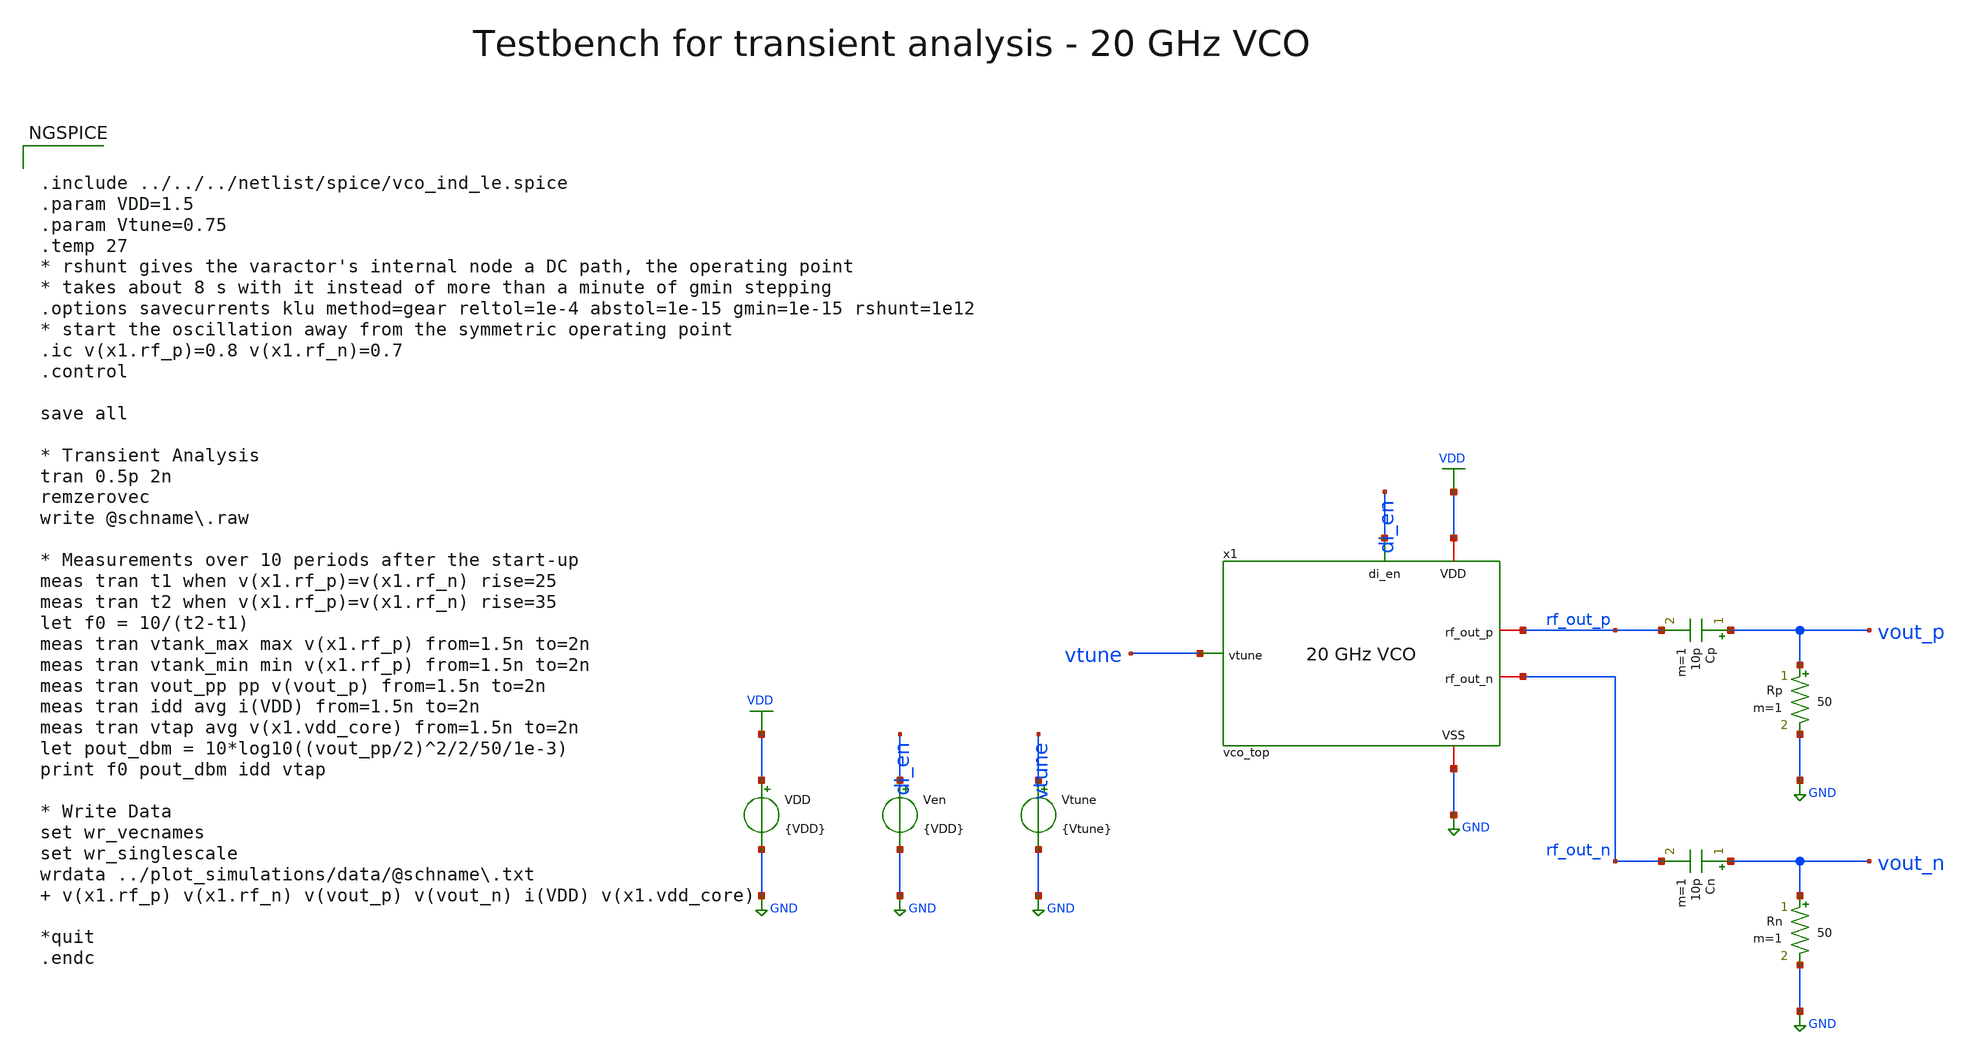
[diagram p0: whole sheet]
** sch_path: macros/vco/testbenches/xschem/vco_top_tb_tran.sch
**.subckt vco_top_tb_tran
x1 di_en VDD GND vtune rf_out_p rf_out_n vco_top
Cp vout_p rf_out_p 10p m=1
Rp vout_p GND 50 m=1
Cn vout_n rf_out_n 10p m=1
Rn vout_n GND 50 m=1
VDD VDD GND {VDD}
Ven di_en GND {VDD}
Vtune vtune GND {Vtune}
**** begin user architecture code


.include ../../../netlist/spice/vco_ind_le.spice
.param VDD=1.5
.param Vtune=0.75
.temp 27
* rshunt gives the varactor's internal node a DC path, the operating point
* takes about 8 s with it instead of more than a minute of gmin stepping
.options savecurrents klu method=gear reltol=1e-4 abstol=1e-15 gmin=1e-15 rshunt=1e12
* start the oscillation away from the symmetric operating point
.ic v(x1.rf_p)=0.8 v(x1.rf_n)=0.7
.control

save all

* Transient Analysis
tran 0.5p 2n
remzerovec
write @schname\.raw

* Measurements over 10 periods after the start-up
meas tran t1 when v(x1.rf_p)=v(x1.rf_n) rise=25
meas tran t2 when v(x1.rf_p)=v(x1.rf_n) rise=35
let f0 = 10/(t2-t1)
meas tran vtank_max max v(x1.rf_p) from=1.5n to=2n
meas tran vtank_min min v(x1.rf_p) from=1.5n to=2n
meas tran vout_pp pp v(vout_p) from=1.5n to=2n
meas tran idd avg i(VDD) from=1.5n to=2n
meas tran vtap avg v(x1.vdd_core) from=1.5n to=2n
let pout_dbm = 10*log10((vout_pp/2)^2/2/50/1e-3)
print f0 pout_dbm idd vtap

* Write Data
set wr_vecnames
set wr_singlescale
wrdata ../plot_simulations/data/@schname\.txt  v(x1.rf_p) v(x1.rf_n) v(vout_p) v(vout_n) i(VDD) v(x1.vdd_core)

*quit
.endc



.lib cornerMOSlv.lib mos_tt
.lib cornerMOShv.lib mos_tt
.lib cornerRES.lib res_typ
.lib cornerCAP.lib cap_typ

**** end user architecture code
**.ends

* expanding   symbol:  vco_top.sym # of pins=6
** sym_path: macros/vco/schematic/xschem/vco_top.sym
** sch_path: macros/vco/schematic/xschem/vco_top.sch
.subckt vco_top di_en VDD VSS vtune rf_out_p rf_out_n
*.iopin VDD
*.iopin VSS
*.ipin di_en
*.ipin vtune
*.iopin rf_out_p
*.iopin rf_out_n
xbias di_en VDD VSS vbg_buf vbn_buf en_b vco_bias
xcore vdd_core VSS vtune rf_p rf_n vco_core
xbuf vbn_buf vbg_buf VDD VSS rf_p rf_n rf_out_p rf_out_n vco_buf
xfeed en_b VDD VSS vdd_core vco_feed
.ends


* expanding   symbol:  vco_bias.sym # of pins=6
** sym_path: macros/vco/schematic/xschem/vco_bias.sym
** sch_path: macros/vco/schematic/xschem/vco_bias.sch
.subckt vco_bias di_en VDD VSS vbg_buf vbn_buf en_b
*.iopin VDD
*.iopin VSS
*.ipin di_en
*.opin en_b
*.iopin vbn_buf
*.iopin vbg_buf
XMPi1 en_b di_en VDD VDD sg13_lv_pmos w=1u l=0.13u ng=1 m=1 mm_ok=1
XMNi1 en_b di_en VSS VSS sg13_lv_nmos w=0.5u l=0.13u ng=1 m=1 mm_ok=1
XMPi2 en en_b VDD VDD sg13_lv_pmos w=1u l=0.13u ng=1 m=1 mm_ok=1
XMNi2 en en_b VSS VSS sg13_lv_nmos w=0.5u l=0.13u ng=1 m=1 mm_ok=1
XMN0 ibias_100u ibias_100u VSS VSS sg13_lv_nmos w=2.5u l=0.5u ng=1 m=1 mm_ok=1
XMNd0 ibias_100u en_b VSS VSS sg13_lv_nmos w=1u l=0.13u ng=1 m=1 mm_ok=1
XRn ibias_100u vbn_buf VSS rhigh w=0.5e-6 l=32e-6 m=1 b=0 mm_ok=1
XMNd1 vbn_buf en_b VSS VSS sg13_lv_nmos w=1u l=0.13u ng=1 m=1 mm_ok=1
XMN1 vbp_ref ibias_100u VSS VSS sg13_lv_nmos w=2.5u l=0.5u ng=1 m=1 mm_ok=1
XMP1 vbp_ref vbp_ref VDD VDD sg13_lv_pmos w=5u l=0.5u ng=1 m=1 mm_ok=1
XMPd vbp_ref en VDD VDD sg13_lv_pmos w=1u l=0.13u ng=1 m=1 mm_ok=1
XMP2 vbg_int vbp_ref VDD VDD sg13_lv_pmos w=5u l=0.5u ng=1 m=1 mm_ok=1
XRg vbg_int nbg VSS rppd w=0.5e-6 l=8.5e-6 m=1 b=0 mm_ok=1
XMN3 nbg nbg VSS VSS sg13_lv_nmos w=2.5u l=0.5u ng=1 m=1 mm_ok=1
XMCn1 VSS vbn_buf VSS VSS sg13_lv_nmos w=40u l=10u ng=5 m=1 mm_ok=1
XMCn2 VSS vbn_buf VSS VSS sg13_lv_nmos w=40u l=10u ng=5 m=1 mm_ok=1
XRf vbg_int vbg_buf VSS rhigh w=0.5e-6 l=32e-6 m=1 b=0 mm_ok=1
XMCg1 VSS vbg_buf VSS VSS sg13_lv_nmos w=40u l=10u ng=5 m=1 mm_ok=1
XMCg2 VSS vbg_buf VSS VSS sg13_lv_nmos w=40u l=10u ng=5 m=1 mm_ok=1
XMDn1 VSS VSS VSS VSS sg13_lv_nmos w=2.5u l=0.5u ng=1 m=1 mm_ok=1
XMDn2 VSS VSS VSS VSS sg13_lv_nmos w=2.5u l=0.5u ng=1 m=1 mm_ok=1
XMDp1 VDD VDD VDD VDD sg13_lv_pmos w=5u l=0.5u ng=1 m=1 mm_ok=1
XMDp2 VDD VDD VDD VDD sg13_lv_pmos w=5u l=0.5u ng=1 m=1 mm_ok=1
XMPb nrb en_b VDD VDD sg13_lv_pmos w=2u l=0.13u ng=1 m=1 mm_ok=1
XMDp4 VDD VDD VDD VDD sg13_lv_pmos w=1u l=0.13u ng=1 m=1 mm_ok=1
XRb nrb ibias_100u VSS rppd w=0.5e-6 l=13.1e-6 m=1 b=0 mm_ok=1
XCg1 vbg_buf VSS cap_cmim w=17.5e-6 l=19.1e-6 m=1 mm_ok=1
XCg2 vbg_buf VSS cap_cmim w=13.6e-6 l=7.28e-6 m=1 mm_ok=1
.ends


* expanding   symbol:  vco_core.sym # of pins=5
** sym_path: macros/vco/schematic/xschem/vco_core.sym
** sch_path: macros/vco/schematic/xschem/vco_core.sch
.subckt vco_core vdd_core VSS vtune rf_p rf_n
*.iopin vdd_core
*.iopin VSS
*.ipin vtune
*.iopin rf_p
*.iopin rf_n
xind rf_p rf_n vdd_core VSS vco_ind
XCct1 vdd_core VSS cap_cmim w=56e-6 l=39e-6 m=1 mm_ok=1
xvar rf_p rf_n vtune VSS vco_var
XM1 rf_p rf_n VSS VSS sg13_lv_nmos w=20u l=0.13u ng=10 m=1 mm_ok=1
XM2 rf_n rf_p VSS VSS sg13_lv_nmos w=20u l=0.13u ng=10 m=1 mm_ok=1
XCct2 vdd_core VSS cap_cmim w=42e-6 l=25.5e-6 m=1 mm_ok=1
.ends


* expanding   symbol:  vco_buf.sym # of pins=8
** sym_path: macros/vco/schematic/xschem/vco_buf.sym
** sch_path: macros/vco/schematic/xschem/vco_buf.sch
.subckt vco_buf vbn_buf vbg_buf VDD VSS rf_p rf_n rf_out_p rf_out_n
*.iopin VDD
*.iopin VSS
*.iopin rf_out_n
*.iopin rf_out_p
*.ipin vbn_buf
*.iopin rf_p
*.iopin rf_n
*.ipin vbg_buf
XMB1 rf_out_n gp tail VSS sg13_lv_nmos w=24u l=0.13u ng=12 m=1 mm_ok=1
XMB2 rf_out_p gn tail VSS sg13_lv_nmos w=24u l=0.13u ng=12 m=1 mm_ok=1
XRL1 VDD rf_out_n VSS rppd w=10e-6 l=1.65e-6 m=1 b=0 mm_ok=1
XRL2 VDD rf_out_p VSS rppd w=10e-6 l=1.65e-6 m=1 b=0 mm_ok=1
XMBt tail vbn_buf VSS VSS sg13_lv_nmos w=150u l=0.5u ng=30 m=1 mm_ok=1
XCc1 gp rf_p cap_cmim w=10e-6 l=10e-6 m=1 mm_ok=1
XCc2 gn rf_n cap_cmim w=10e-6 l=10e-6 m=1 mm_ok=1
XRb1 vbg_buf gp VSS rhigh w=0.5e-6 l=8e-6 m=1 b=0 mm_ok=1
XRb2 vbg_buf gn VSS rhigh w=0.5e-6 l=8e-6 m=1 b=0 mm_ok=1
.ends


* expanding   symbol:  vco_feed.sym # of pins=4
** sym_path: macros/vco/schematic/xschem/vco_feed.sym
** sch_path: macros/vco/schematic/xschem/vco_feed.sch
.subckt vco_feed en_b VDD VSS vdd_core
*.iopin VDD
*.iopin VSS
*.ipin en_b
*.iopin vdd_core
XMPs n1 en_b VDD VDD sg13_lv_pmos w=96u l=0.13u ng=32 m=1 mm_ok=1
XRct n1 vdd_core VSS rppd w=17.3e-6 l=8.8e-6 m=1 b=0 mm_ok=1
.ends


* expanding   symbol:  vco_ind.sym # of pins=4
** sym_path: macros/vco/schematic/xschem/vco_ind.sym
** sch_path: macros/vco/schematic/xschem/vco_ind.sch
.subckt vco_ind la lb lc VSS
*.iopin la
*.iopin lc
*.iopin lb
*.iopin VSS
XL1 la lc lb VSS inductor3 w=4e-6 s=4e-6 d=52e-6 nr_r=2 m=1
x1 la lb lc vco_ind_le
.ends


* expanding   symbol:  vco_var.sym # of pins=4
** sym_path: macros/vco/schematic/xschem/vco_var.sym
** sch_path: macros/vco/schematic/xschem/vco_var.sch
.subckt vco_var rf_p rf_n vtune VSS
*.ipin vtune
*.iopin rf_p
*.iopin rf_n
*.iopin VSS
XCvar1 rf_p vtune rf_n VSS sg13_hv_svaricap w=3.74u l=0.3u Nx=7 mm_ok=1
XCvar2 rf_p vtune rf_n VSS sg13_hv_svaricap w=3.74u l=0.3u Nx=7 mm_ok=1
XCvar3 rf_p vtune rf_n VSS sg13_hv_svaricap w=3.74u l=0.3u Nx=7 mm_ok=1
.ends

.GLOBAL VDD
.GLOBAL GND
.end
